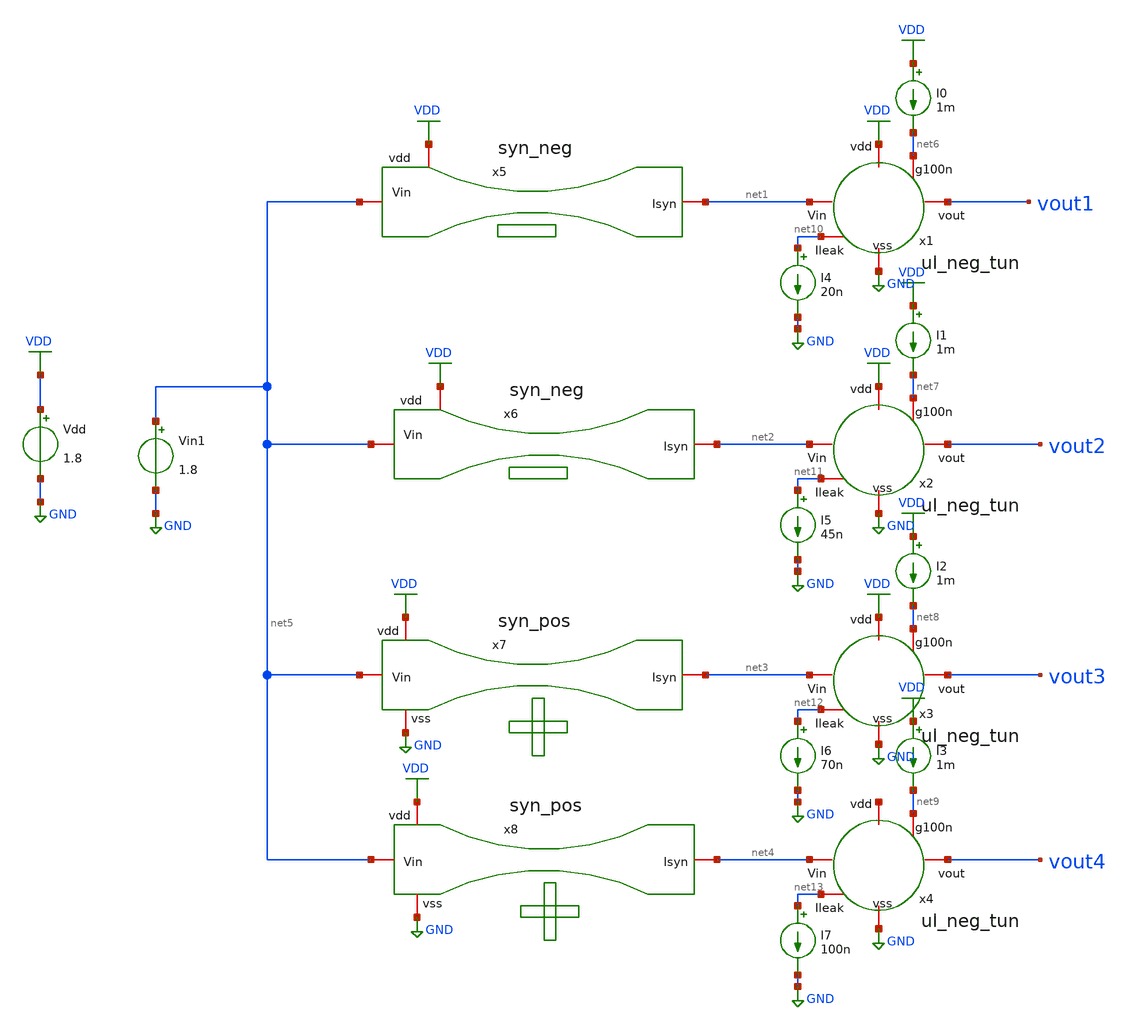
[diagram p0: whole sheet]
** sch_path: Neuron/ultralif/untitled.sch
**.subckt untitled
x1 net1 VDD net6 vout1 net10 GND ul_neg_tun
x2 net2 VDD net7 vout2 net11 GND ul_neg_tun
x3 net3 VDD net8 vout3 net12 GND ul_neg_tun
x4 net4 net14 net9 vout4 net13 GND ul_neg_tun
x5 VDD net5 net1 syn_neg
x6 VDD net5 net2 syn_neg
x7 GND net5 net3 VDD syn_pos
x8 GND net5 net4 VDD syn_pos
Vdd VDD GND 1.8
Vin1 net5 GND 1.8
I0 VDD net6 1m
I1 VDD net7 1m
I2 VDD net8 1m
I3 VDD net9 1m
I4 net10 GND 20n
I5 net11 GND 45n
I6 net12 GND 70n
I7 net13 GND 100n
**.ends

* expanding   symbol:  ul_neg_tun.sym # of pins=6
** sym_path: Neuron/ultralif/ul_neg_tun.sym
** sch_path: Neuron/ultralif/ul_neg_tun.sch
.subckt ul_neg_tun Iext vdd g100n vout Ileak vss
*.iopin Iext
*.iopin vout
*.iopin vss
*.iopin Ileak
*.iopin vdd
*.iopin g100n
XM1 Ileak Ileak vm vdd sky130_fd_pr__pfet_01v8 L=10 W=1 nf=1 ad='int((nf+1)/2) * W/nf * 0.29' as='int((nf+2)/2) * W/nf * 0.29'
+ pd='2*int((nf+1)/2) * (W/nf + 0.29)' ps='2*int((nf+2)/2) * (W/nf + 0.29)' nrd='0.29 / W' nrs='0.29 / W'
+ sa=0 sb=0 sd=0 mult=1 m=1
XM2 Ileak net1 vm vdd sky130_fd_pr__pfet_01v8 L=0.15 W=1.5 nf=1 ad='int((nf+1)/2) * W/nf * 0.29' as='int((nf+2)/2) * W/nf * 0.29'
+ pd='2*int((nf+1)/2) * (W/nf + 0.29)' ps='2*int((nf+2)/2) * (W/nf + 0.29)' nrd='0.29 / W' nrs='0.29 / W'
+ sa=0 sb=0 sd=0 mult=1 m=1
XM3 net1 net1 vm vdd sky130_fd_pr__pfet_01v8 L=0.15 W=15 nf=1 ad='int((nf+1)/2) * W/nf * 0.29' as='int((nf+2)/2) * W/nf * 0.29'
+ pd='2*int((nf+1)/2) * (W/nf + 0.29)' ps='2*int((nf+2)/2) * (W/nf + 0.29)' nrd='0.29 / W' nrs='0.29 / W'
+ sa=0 sb=0 sd=0 mult=1 m=1
XM4 net1 Ileak vss vss sky130_fd_pr__nfet_01v8 L=4 W=1 nf=1 ad='int((1 + 1)/2) * 1 / 1 * 0.29' as='int((1 + 2)/2) * 1 / 1 * 0.29'
+ pd='2*int((1 + 1)/2) * (1 / 1 + 0.29)' ps='2*int((1 + 2)/2) * (1 / 1 + 0.29)' nrd='0.29 / 1 ' nrs='0.29 / 1 '
+ sa=0 sb=0 sd=0 mult=1 m=1
C1 vm vss 1p m=1
XM5 vout_n Ileak vss vss sky130_fd_pr__nfet_01v8 L=0.15 W=1 nf=1 ad='int((1 + 1)/2) * 1 / 1 * 0.29' as='int((1 + 2)/2) * 1 / 1 * 0.29'
+ pd='2*int((1 + 1)/2) * (1 / 1 + 0.29)' ps='2*int((1 + 2)/2) * (1 / 1 + 0.29)' nrd='0.29 / 1 ' nrs='0.29 / 1 '
+ sa=0 sb=0 sd=0 mult=1 m=1
XM6 vout_n g100n vdd vdd sky130_fd_pr__pfet_01v8 L=0.15 W=2 nf=1 ad='int((nf+1)/2) * W/nf * 0.29' as='int((nf+2)/2) * W/nf * 0.29'
+ pd='2*int((nf+1)/2) * (W/nf + 0.29)' ps='2*int((nf+2)/2) * (W/nf + 0.29)' nrd='0.29 / W' nrs='0.29 / W'
+ sa=0 sb=0 sd=0 mult=1 m=1
XM7 vout vout_n vss vss sky130_fd_pr__nfet_01v8 L=0.15 W=1 nf=1 ad='int((1 + 1)/2) * 1 / 1 * 0.29' as='int((1 + 2)/2) * 1 / 1 * 0.29'
+ pd='2*int((1 + 1)/2) * (1 / 1 + 0.29)' ps='2*int((1 + 2)/2) * (1 / 1 + 0.29)' nrd='0.29 / 1 ' nrs='0.29 / 1 '
+ sa=0 sb=0 sd=0 mult=1 m=1
XM8 vout vout_n vdd vdd sky130_fd_pr__pfet_01v8 L=0.15 W=2 nf=1 ad='int((nf+1)/2) * W/nf * 0.29' as='int((nf+2)/2) * W/nf * 0.29'
+ pd='2*int((nf+1)/2) * (W/nf + 0.29)' ps='2*int((nf+2)/2) * (W/nf + 0.29)' nrd='0.29 / W' nrs='0.29 / W'
+ sa=0 sb=0 sd=0 mult=1 m=1
XM9 vm Ileak Iext vdd sky130_fd_pr__pfet_01v8 L=0.15 W=2 nf=1 ad='int((nf+1)/2) * W/nf * 0.29' as='int((nf+2)/2) * W/nf * 0.29'
+ pd='2*int((nf+1)/2) * (W/nf + 0.29)' ps='2*int((nf+2)/2) * (W/nf + 0.29)' nrd='0.29 / W' nrs='0.29 / W'
+ sa=0 sb=0 sd=0 mult=1 m=1
.ends


* expanding   symbol:  syn_neg.sym # of pins=3
** sym_path: Neuron/ultralif/syn_neg.sym
** sch_path: Neuron/ultralif/syn_neg.sch
.subckt syn_neg vdd Vin Isyn
*.iopin Vin
*.iopin Isyn
*.iopin vdd
XM10 Isyn Vin vx vdd sky130_fd_pr__pfet_01v8 L=30 W=0.5 nf=1 ad='int((nf+1)/2) * W/nf * 0.29' as='int((nf+2)/2) * W/nf * 0.29'
+ pd='2*int((nf+1)/2) * (W/nf + 0.29)' ps='2*int((nf+2)/2) * (W/nf + 0.29)' nrd='0.29 / W' nrs='0.29 / W'
+ sa=0 sb=0 sd=0 mult=1 m=1
XM1 vx Vin vdd vdd sky130_fd_pr__pfet_01v8 L=30 W=0.5 nf=1 ad='int((nf+1)/2) * W/nf * 0.29' as='int((nf+2)/2) * W/nf * 0.29'
+ pd='2*int((nf+1)/2) * (W/nf + 0.29)' ps='2*int((nf+2)/2) * (W/nf + 0.29)' nrd='0.29 / W' nrs='0.29 / W'
+ sa=0 sb=0 sd=0 mult=1 m=1
.ends


* expanding   symbol:  syn_pos.sym # of pins=4
** sym_path: Neuron/ultralif/syn_pos.sym
** sch_path: Neuron/ultralif/syn_pos.sch
.subckt syn_pos vss Vin Isyn vdd
*.iopin Vin
*.iopin vdd
*.iopin vss
*.iopin Isyn
XM9 Isyn vx vdd vdd sky130_fd_pr__pfet_01v8 L=1 W=0.5 nf=1 ad='int((nf+1)/2) * W/nf * 0.29' as='int((nf+2)/2) * W/nf * 0.29'
+ pd='2*int((nf+1)/2) * (W/nf + 0.29)' ps='2*int((nf+2)/2) * (W/nf + 0.29)' nrd='0.29 / W' nrs='0.29 / W'
+ sa=0 sb=0 sd=0 mult=1 m=1
XM10 vx vx vdd vdd sky130_fd_pr__pfet_01v8 L=0.15 W=0.5 nf=1 ad='int((nf+1)/2) * W/nf * 0.29' as='int((nf+2)/2) * W/nf * 0.29'
+ pd='2*int((nf+1)/2) * (W/nf + 0.29)' ps='2*int((nf+2)/2) * (W/nf + 0.29)' nrd='0.29 / W' nrs='0.29 / W'
+ sa=0 sb=0 sd=0 mult=5 m=5
XM12 vx Vin vss vss sky130_fd_pr__nfet_01v8 L=1 W=0.4 nf=1 ad='int((1 + 1)/2) * 0.4 / 1 * 0.29' as='int((1 + 2)/2) * 0.4 / 1 * 0.29'
+ pd='2*int((1 + 1)/2) * (0.4 / 1 + 0.29)' ps='2*int((1 + 2)/2) * (0.4 / 1 + 0.29)' nrd='0.29 / 0.4 ' nrs='0.29 / 0.4 '
+ sa=0 sb=0 sd=0 mult=1 m=1
.ends

.GLOBAL GND
.GLOBAL VDD
.end
